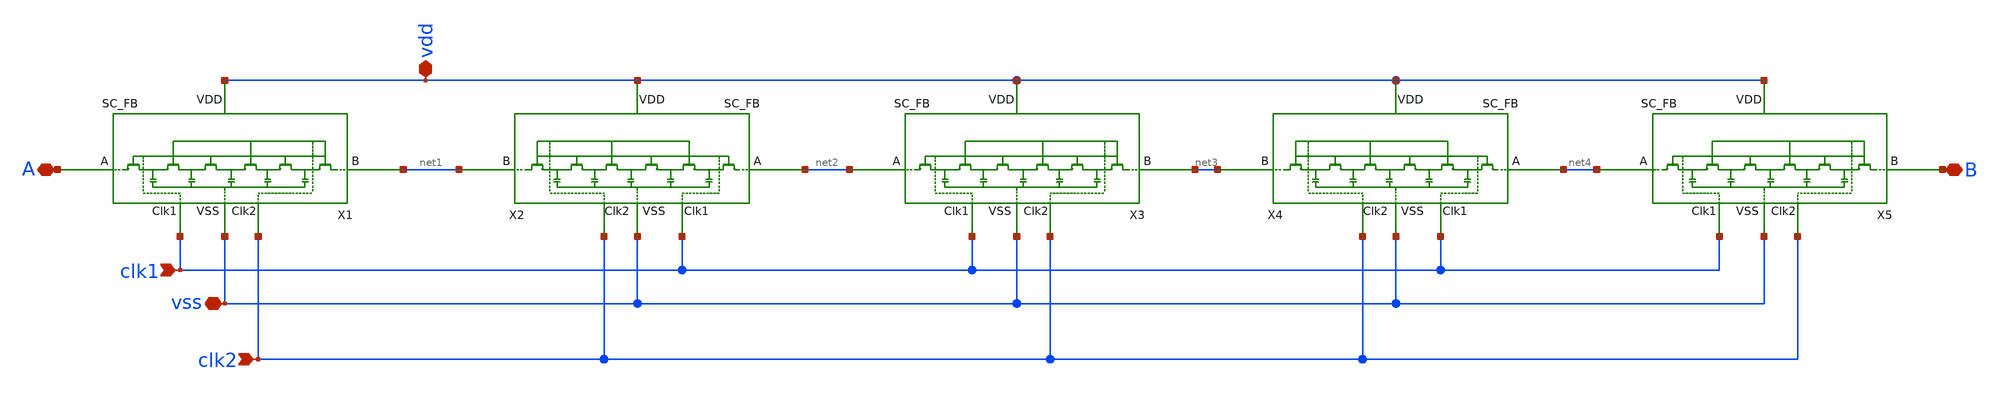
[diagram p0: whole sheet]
** sch_path: 225G_SC_res.sch
**.subckt 225G_SC_res A B vss vdd clk2 clk1
*.iopin A
*.iopin B
*.iopin vss
*.iopin vdd
*.ipin clk2
*.ipin clk1
X1 A net1 clk1 clk2 vss vdd SC_FB
X2 net2 net1 clk1 clk2 vss vdd SC_FB
X3 net2 net3 clk1 clk2 vss vdd SC_FB
X4 net4 net3 clk1 clk2 vss vdd SC_FB
X5 net4 B clk1 clk2 vss vdd SC_FB
**.ends

* expanding   symbol:  LNA/SC_FB.sym # of pins=6
** sym_path: SC_FB.sym
** sch_path: SC_FB.sch
.subckt SC_FB A B Clk1_SC Clk2_SC VSS_SC VDD_SC
*.iopin A
*.ipin Clk1_SC
*.ipin Clk2_SC
*.iopin VSS_SC
*.iopin B
*.iopin VDD_SC
XC1 i5 VSS_SC sky130_fd_pr__cap_mim_m3_2 W=2 L=2 MF=2 m=2
XC2 i4 VSS_SC sky130_fd_pr__cap_mim_m3_2 W=2 L=2 MF=2 m=2
XC3 i3 VSS_SC sky130_fd_pr__cap_mim_m3_2 W=2 L=2 MF=2 m=2
XC4 i2 VSS_SC sky130_fd_pr__cap_mim_m3_2 W=2 L=2 MF=2 m=2
XM1 i5 Clk1_SC i4 VDD_SC sky130_fd_pr__pfet_01v8_hvt L=0.15 W=0.54 nf=1 ad='int((nf+1)/2) * W/nf * 0.29'
+ as='int((nf+2)/2) * W/nf * 0.29' pd='2*int((nf+1)/2) * (W/nf + 0.29)' ps='2*int((nf+2)/2) * (W/nf + 0.29)'
+ nrd='0.29 / W' nrs='0.29 / W' sa=0 sb=0 sd=0 mult=1 m=1
XM2 i4 Clk2_SC i3 VDD_SC sky130_fd_pr__pfet_01v8_hvt L=0.15 W=0.54 nf=1 ad='int((nf+1)/2) * W/nf * 0.29'
+ as='int((nf+2)/2) * W/nf * 0.29' pd='2*int((nf+1)/2) * (W/nf + 0.29)' ps='2*int((nf+2)/2) * (W/nf + 0.29)'
+ nrd='0.29 / W' nrs='0.29 / W' sa=0 sb=0 sd=0 mult=1 m=1
XM3 i3 Clk1_SC i2 VDD_SC sky130_fd_pr__pfet_01v8_hvt L=0.15 W=0.54 nf=1 ad='int((nf+1)/2) * W/nf * 0.29'
+ as='int((nf+2)/2) * W/nf * 0.29' pd='2*int((nf+1)/2) * (W/nf + 0.29)' ps='2*int((nf+2)/2) * (W/nf + 0.29)'
+ nrd='0.29 / W' nrs='0.29 / W' sa=0 sb=0 sd=0 mult=1 m=1
XM4 i2 Clk2_SC i1 VDD_SC sky130_fd_pr__pfet_01v8_hvt L=0.15 W=0.54 nf=1 ad='int((nf+1)/2) * W/nf * 0.29'
+ as='int((nf+2)/2) * W/nf * 0.29' pd='2*int((nf+1)/2) * (W/nf + 0.29)' ps='2*int((nf+2)/2) * (W/nf + 0.29)'
+ nrd='0.29 / W' nrs='0.29 / W' sa=0 sb=0 sd=0 mult=1 m=1
XM5 i1 Clk1_SC A VDD_SC sky130_fd_pr__pfet_01v8_hvt L=0.15 W=0.54 nf=1 ad='int((nf+1)/2) * W/nf * 0.29'
+ as='int((nf+2)/2) * W/nf * 0.29' pd='2*int((nf+1)/2) * (W/nf + 0.29)' ps='2*int((nf+2)/2) * (W/nf + 0.29)'
+ nrd='0.29 / W' nrs='0.29 / W' sa=0 sb=0 sd=0 mult=1 m=1
XM6 B Clk2_SC i5 VDD_SC sky130_fd_pr__pfet_01v8_hvt L=0.15 W=0.54 nf=1 ad='int((nf+1)/2) * W/nf * 0.29'
+ as='int((nf+2)/2) * W/nf * 0.29' pd='2*int((nf+1)/2) * (W/nf + 0.29)' ps='2*int((nf+2)/2) * (W/nf + 0.29)'
+ nrd='0.29 / W' nrs='0.29 / W' sa=0 sb=0 sd=0 mult=1 m=1
XC5 i1 VSS_SC sky130_fd_pr__cap_mim_m3_2 W=2 L=2 MF=2 m=2
.ends

.end
